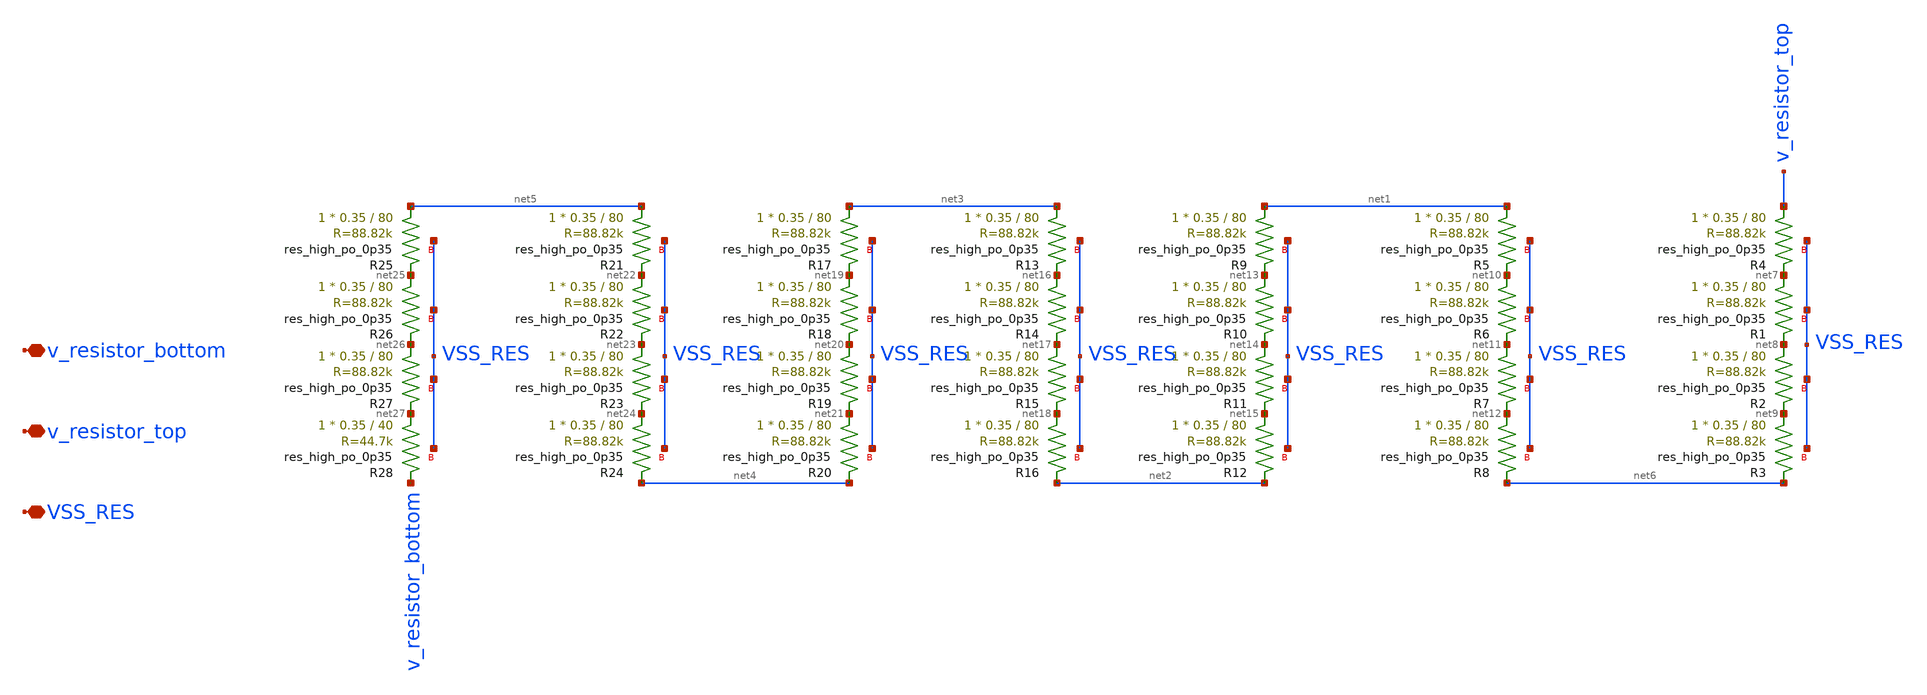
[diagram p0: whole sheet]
** sch_path: core_bias_res.sch
**.subckt core_bias_res v_resistor_bottom v_resistor_top VSS_RES
*.iopin v_resistor_bottom
*.iopin v_resistor_top
*.iopin VSS_RES
XR4 v_resistor_top net7 VSS_RES sky130_fd_pr__res_high_po_0p35 L=80 mult=1 m=1
XR1 net7 net8 VSS_RES sky130_fd_pr__res_high_po_0p35 L=80 mult=1 m=1
XR2 net8 net9 VSS_RES sky130_fd_pr__res_high_po_0p35 L=80 mult=1 m=1
XR3 net9 net6 VSS_RES sky130_fd_pr__res_high_po_0p35 L=80 mult=1 m=1
XR5 net1 net10 VSS_RES sky130_fd_pr__res_high_po_0p35 L=80 mult=1 m=1
XR6 net10 net11 VSS_RES sky130_fd_pr__res_high_po_0p35 L=80 mult=1 m=1
XR7 net11 net12 VSS_RES sky130_fd_pr__res_high_po_0p35 L=80 mult=1 m=1
XR8 net12 net6 VSS_RES sky130_fd_pr__res_high_po_0p35 L=80 mult=1 m=1
XR9 net1 net13 VSS_RES sky130_fd_pr__res_high_po_0p35 L=80 mult=1 m=1
XR10 net13 net14 VSS_RES sky130_fd_pr__res_high_po_0p35 L=80 mult=1 m=1
XR11 net14 net15 VSS_RES sky130_fd_pr__res_high_po_0p35 L=80 mult=1 m=1
XR12 net15 net2 VSS_RES sky130_fd_pr__res_high_po_0p35 L=80 mult=1 m=1
XR13 net3 net16 VSS_RES sky130_fd_pr__res_high_po_0p35 L=80 mult=1 m=1
XR14 net16 net17 VSS_RES sky130_fd_pr__res_high_po_0p35 L=80 mult=1 m=1
XR15 net17 net18 VSS_RES sky130_fd_pr__res_high_po_0p35 L=80 mult=1 m=1
XR16 net18 net2 VSS_RES sky130_fd_pr__res_high_po_0p35 L=80 mult=1 m=1
XR17 net3 net19 VSS_RES sky130_fd_pr__res_high_po_0p35 L=80 mult=1 m=1
XR18 net19 net20 VSS_RES sky130_fd_pr__res_high_po_0p35 L=80 mult=1 m=1
XR19 net20 net21 VSS_RES sky130_fd_pr__res_high_po_0p35 L=80 mult=1 m=1
XR20 net21 net4 VSS_RES sky130_fd_pr__res_high_po_0p35 L=80 mult=1 m=1
XR21 net5 net22 VSS_RES sky130_fd_pr__res_high_po_0p35 L=80 mult=1 m=1
XR22 net22 net23 VSS_RES sky130_fd_pr__res_high_po_0p35 L=80 mult=1 m=1
XR23 net23 net24 VSS_RES sky130_fd_pr__res_high_po_0p35 L=80 mult=1 m=1
XR24 net24 net4 VSS_RES sky130_fd_pr__res_high_po_0p35 L=80 mult=1 m=1
XR25 net5 net25 VSS_RES sky130_fd_pr__res_high_po_0p35 L=80 mult=1 m=1
XR26 net25 net26 VSS_RES sky130_fd_pr__res_high_po_0p35 L=80 mult=1 m=1
XR27 net26 net27 VSS_RES sky130_fd_pr__res_high_po_0p35 L=80 mult=1 m=1
XR28 net27 v_resistor_bottom VSS_RES sky130_fd_pr__res_high_po_0p35 L=40 mult=1 m=1
**.ends
.end
